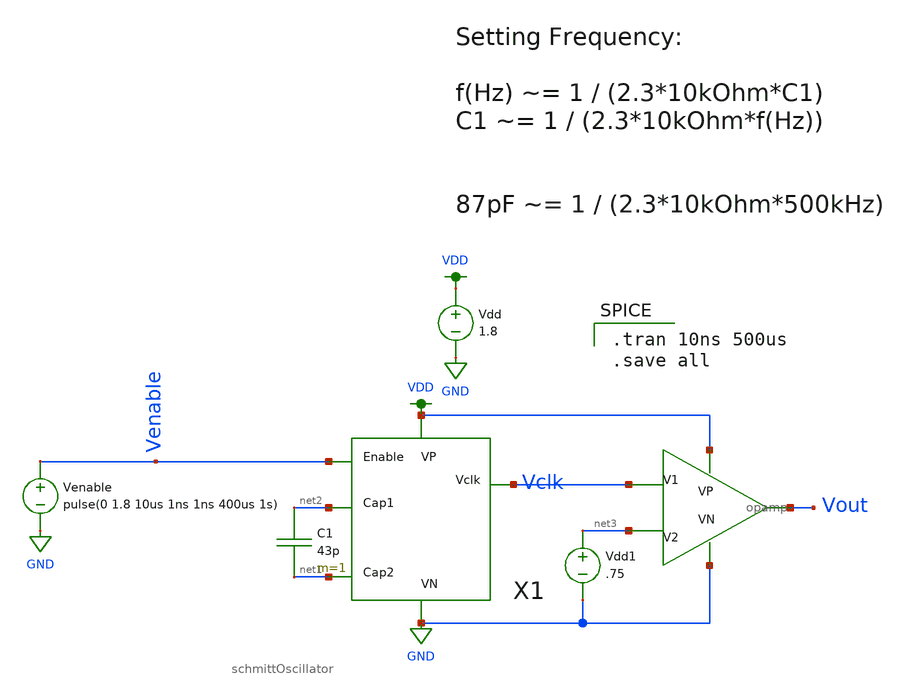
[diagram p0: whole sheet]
** sch_path: schematics/oscillatorTestbench.sch
**.subckt oscillatorTestbench
Vdd VDD GND 1.8
Venable Venable GND pulse(0 1.8 10us 1ns 1ns 400us 1s)
X1 Venable net2 net1 VDD GND Vclk schmittOscillator
C1 net2 net1 43p m=1
X2 Vclk net3 VDD GND Vout opamp
Vdd1 net3 GND .75
**** begin user architecture code

.option wnflag=1
.lib ~/skywater/skywater-pdk/libraries/sky130_fd_pr_ngspice/latest/models/sky130.lib.spice tt


.tran 10ns 500us
.save all

**** end user architecture code
**.ends
.GLOBAL GND
.GLOBAL VDD
.end
